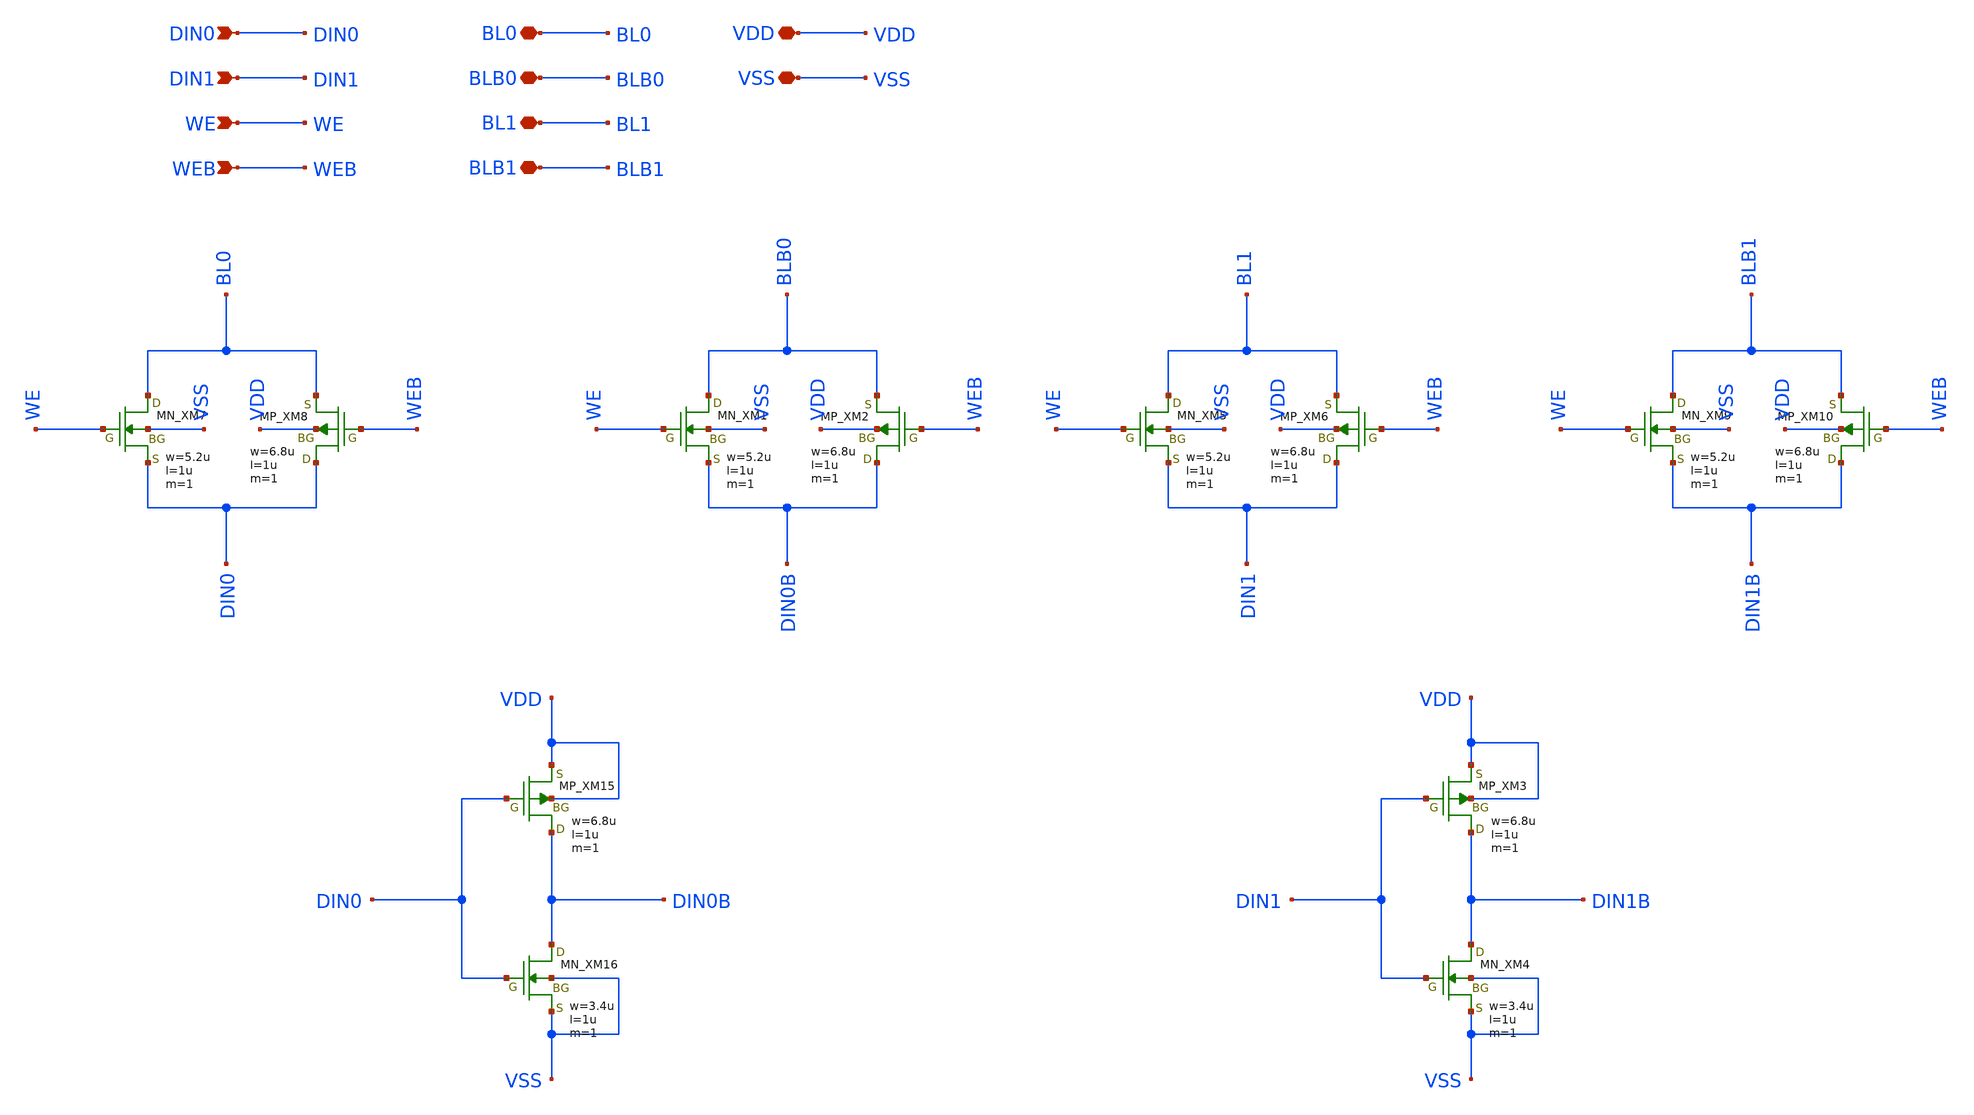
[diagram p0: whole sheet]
** sch_path: array/2word_x_2bit/write_driver.sch
**.subckt write_driver DIN0 DIN1 WE WEB BL0 BLB0 BL1 BLB1 VDD VSS
*.ipin DIN0
*.ipin DIN1
*.ipin WE
*.ipin WEB
*.iopin BL0
*.iopin BLB0
*.iopin BL1
*.iopin BLB1
*.iopin VDD
*.iopin VSS
XXM15 DIN0B DIN0 VDD VDD PMOS w=6.8u l=1u nrd=0 nrs=0 m=1
XXM16 DIN0B DIN0 VSS VSS NMOS w=3.4u l=1u nrd=0 nrs=0 m=1
XXM7 BL0 WE DIN0 VSS NMOS w=5.2u l=1u nrd=0 nrs=0 m=1
XXM8 DIN0 WEB BL0 VDD PMOS w=6.8u l=1u nrd=0 nrs=0 m=1
XXM1 BLB0 WE DIN0B VSS NMOS w=5.2u l=1u nrd=0 nrs=0 m=1
XXM2 DIN0B WEB BLB0 VDD PMOS w=6.8u l=1u nrd=0 nrs=0 m=1
XXM3 DIN1B DIN1 VDD VDD PMOS w=6.8u l=1u nrd=0 nrs=0 m=1
XXM4 DIN1B DIN1 VSS VSS NMOS w=3.4u l=1u nrd=0 nrs=0 m=1
XXM5 BL1 WE DIN1 VSS NMOS w=5.2u l=1u nrd=0 nrs=0 m=1
XXM6 DIN1 WEB BL1 VDD PMOS w=6.8u l=1u nrd=0 nrs=0 m=1
XXM9 BLB1 WE DIN1B VSS NMOS w=5.2u l=1u nrd=0 nrs=0 m=1
XXM10 DIN1B WEB BLB1 VDD PMOS w=6.8u l=1u nrd=0 nrs=0 m=1
**.ends
.end
